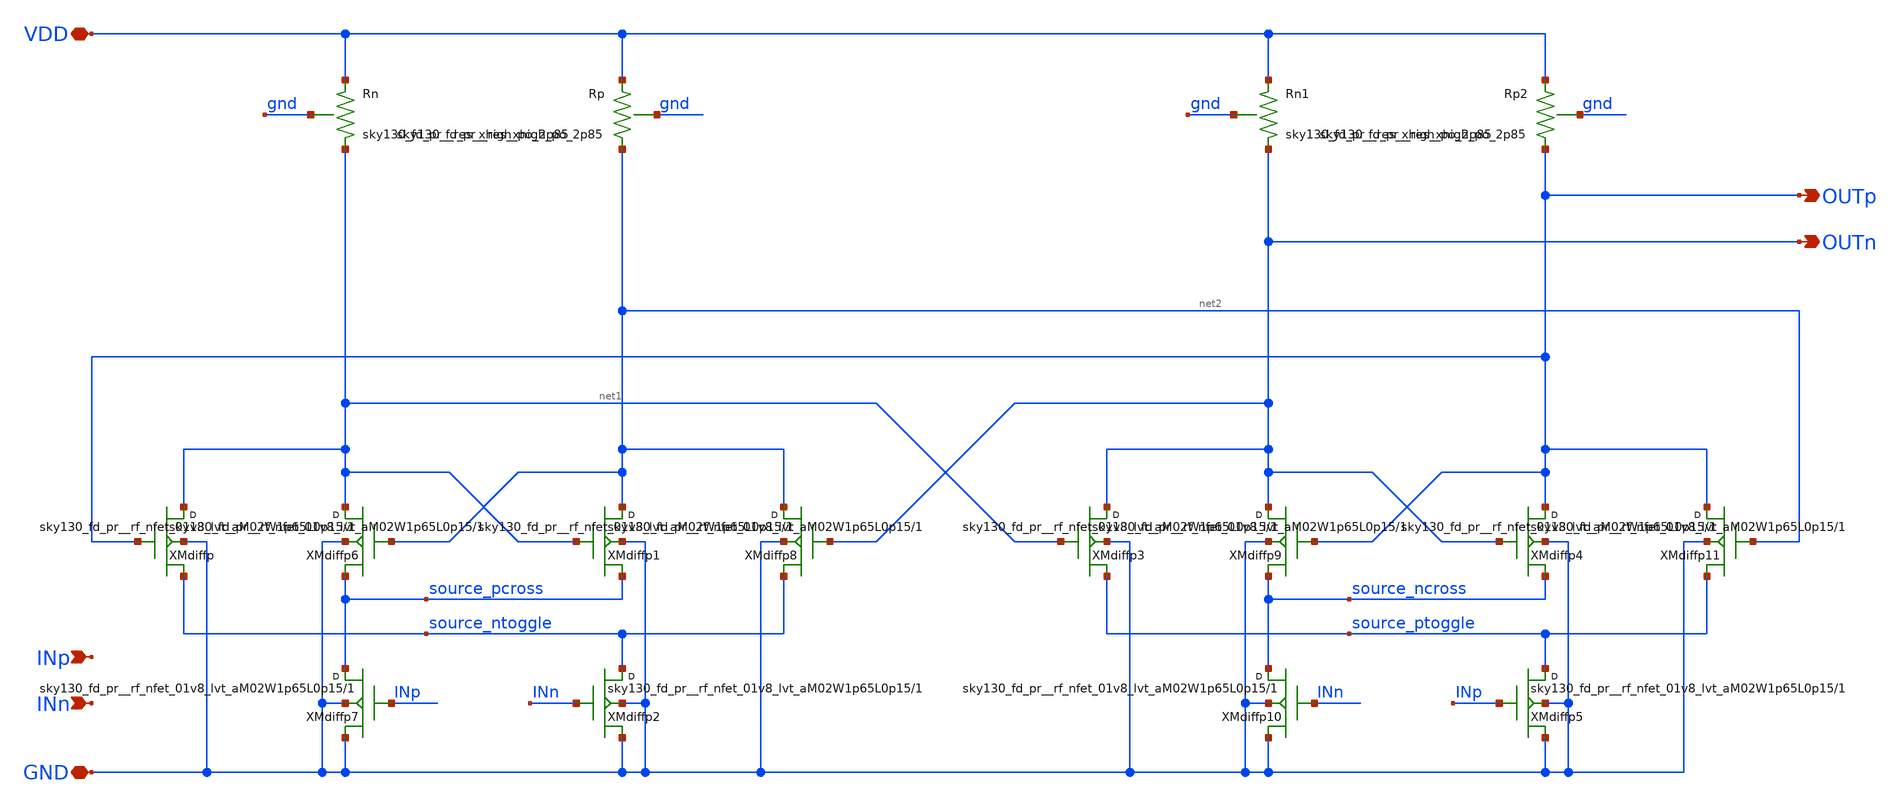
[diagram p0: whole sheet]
** sch_path: design/divider_cml/divider_cml.sch
**.subckt divider_cml INn OUTp VDD GND OUTn INp
*.ipin INn
*.opin OUTp
*.iopin VDD
*.iopin GND
*.opin OUTn
*.ipin INp
XXMdiffp net1 OUTp source_ntoggle GND sky130_fd_pr__rf_nfet_01v8_lvt_aM02W1p65L0p15 m=1
XXMdiffp1 net2 net1 source_pcross GND sky130_fd_pr__rf_nfet_01v8_lvt_aM02W1p65L0p15 m=1
XXMdiffp2 source_ntoggle INn GND GND sky130_fd_pr__rf_nfet_01v8_lvt_aM02W1p65L0p15 m=1
XXMdiffp3 OUTn net1 source_ptoggle GND sky130_fd_pr__rf_nfet_01v8_lvt_aM02W1p65L0p15 m=1
XXMdiffp4 OUTp OUTn source_ncross GND sky130_fd_pr__rf_nfet_01v8_lvt_aM02W1p65L0p15 m=1
XXMdiffp5 source_ptoggle INp GND GND sky130_fd_pr__rf_nfet_01v8_lvt_aM02W1p65L0p15 m=1
XXMdiffp6 net1 net2 source_pcross GND sky130_fd_pr__rf_nfet_01v8_lvt_aM02W1p65L0p15 m=1
XXMdiffp7 source_pcross INp GND GND sky130_fd_pr__rf_nfet_01v8_lvt_aM02W1p65L0p15 m=1
XXMdiffp8 net2 OUTn source_ntoggle GND sky130_fd_pr__rf_nfet_01v8_lvt_aM02W1p65L0p15 m=1
XXMdiffp9 OUTn OUTp source_ncross GND sky130_fd_pr__rf_nfet_01v8_lvt_aM02W1p65L0p15 m=1
XXMdiffp10 source_ncross INn GND GND sky130_fd_pr__rf_nfet_01v8_lvt_aM02W1p65L0p15 m=1
XXMdiffp11 OUTp net2 source_ptoggle GND sky130_fd_pr__rf_nfet_01v8_lvt_aM02W1p65L0p15 m=1
XRn VDD net1 gnd sky130_fd_pr__res_xhigh_po_2p85 m=1
XRp VDD net2 gnd sky130_fd_pr__res_xhigh_po_2p85 m=1
XRn1 VDD OUTn gnd sky130_fd_pr__res_xhigh_po_2p85 m=1
XRp2 VDD OUTp gnd sky130_fd_pr__res_xhigh_po_2p85 m=1
**.ends
.end
